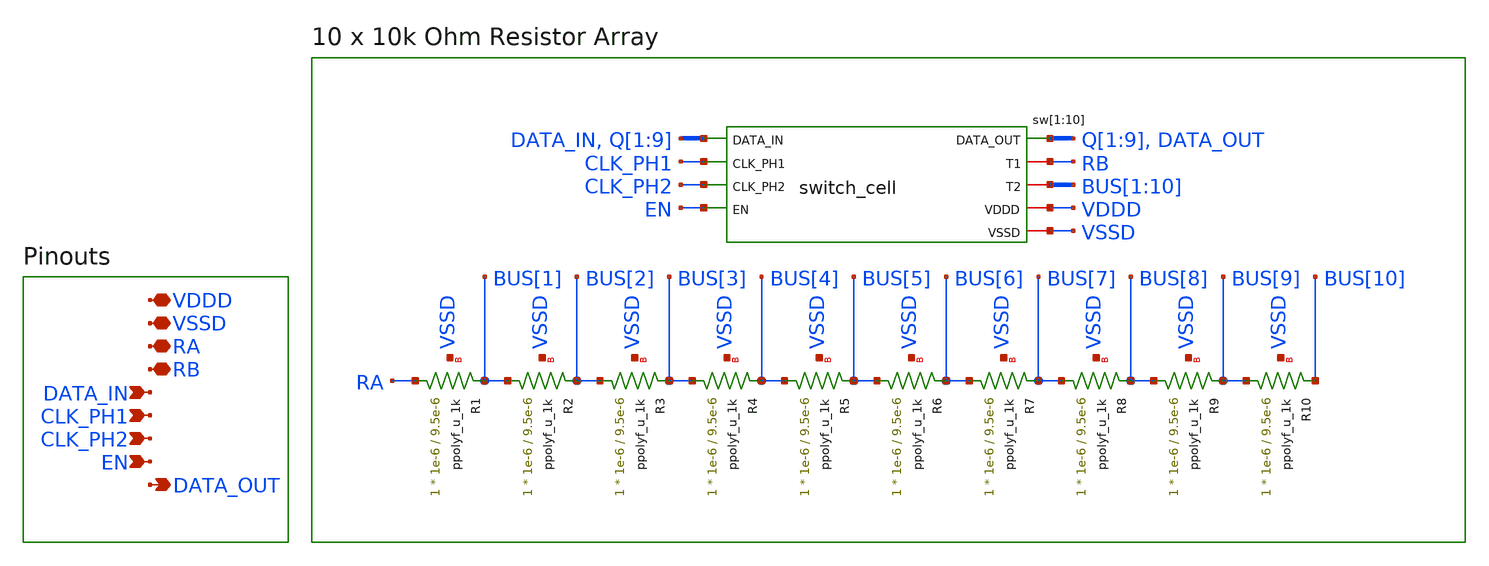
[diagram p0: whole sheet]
** sch_path: designs/libs/core_passive_array/array_res_10x10k/array_res_10x10k.sch
**.subckt array_res_10x10k RA RB VDDD VSSD DATA_IN CLK_PH1 CLK_PH2 EN DATA_OUT
*.iopin RA
*.iopin RB
*.iopin VDDD
*.iopin VSSD
*.ipin DATA_IN
*.ipin CLK_PH1
*.ipin CLK_PH2
*.ipin EN
*.opin DATA_OUT
XR1 RA BUS[1] VSSD ppolyf_u_1k r_width=1e-6 r_length=9.5e-6 m=1
XR2 BUS[1] BUS[2] VSSD ppolyf_u_1k r_width=1e-6 r_length=9.5e-6 m=1
XR3 BUS[2] BUS[3] VSSD ppolyf_u_1k r_width=1e-6 r_length=9.5e-6 m=1
XR4 BUS[3] BUS[4] VSSD ppolyf_u_1k r_width=1e-6 r_length=9.5e-6 m=1
XR5 BUS[4] BUS[5] VSSD ppolyf_u_1k r_width=1e-6 r_length=9.5e-6 m=1
XR6 BUS[5] BUS[6] VSSD ppolyf_u_1k r_width=1e-6 r_length=9.5e-6 m=1
XR7 BUS[6] BUS[7] VSSD ppolyf_u_1k r_width=1e-6 r_length=9.5e-6 m=1
XR8 BUS[7] BUS[8] VSSD ppolyf_u_1k r_width=1e-6 r_length=9.5e-6 m=1
XR9 BUS[8] BUS[9] VSSD ppolyf_u_1k r_width=1e-6 r_length=9.5e-6 m=1
XR10 BUS[9] BUS[10] VSSD ppolyf_u_1k r_width=1e-6 r_length=9.5e-6 m=1
sw[1] DATA_IN CLK_PH1 CLK_PH2 EN Q[1] RB BUS[1] VDDD VSSD switch_cell
sw[2] Q[1] CLK_PH1 CLK_PH2 EN Q[2] RB BUS[2] VDDD VSSD switch_cell
sw[3] Q[2] CLK_PH1 CLK_PH2 EN Q[3] RB BUS[3] VDDD VSSD switch_cell
sw[4] Q[3] CLK_PH1 CLK_PH2 EN Q[4] RB BUS[4] VDDD VSSD switch_cell
sw[5] Q[4] CLK_PH1 CLK_PH2 EN Q[5] RB BUS[5] VDDD VSSD switch_cell
sw[6] Q[5] CLK_PH1 CLK_PH2 EN Q[6] RB BUS[6] VDDD VSSD switch_cell
sw[7] Q[6] CLK_PH1 CLK_PH2 EN Q[7] RB BUS[7] VDDD VSSD switch_cell
sw[8] Q[7] CLK_PH1 CLK_PH2 EN Q[8] RB BUS[8] VDDD VSSD switch_cell
sw[9] Q[8] CLK_PH1 CLK_PH2 EN Q[9] RB BUS[9] VDDD VSSD switch_cell
sw[10] Q[9] CLK_PH1 CLK_PH2 EN DATA_OUT RB BUS[10] VDDD VSSD switch_cell
**.ends

* expanding   symbol:  libs/core_switch_matrix/switch_cell/switch_cell.sym # of pins=9
** sym_path: designs/libs/core_switch_matrix/switch_cell/switch_cell.sym
** sch_path: designs/libs/core_switch_matrix/switch_cell/switch_cell.sch
.subckt switch_cell DATA_IN CLK_PH1 CLK_PH2 EN DATA_OUT T1 T2 VDDD VSSD
*.ipin DATA_IN
*.ipin CLK_PH1
*.ipin CLK_PH2
*.opin DATA_OUT
*.iopin VDDD
*.iopin VSSD
*.ipin EN
*.iopin T1
*.iopin T2
x1 DATA_IN CLK_PH1 CLK_PH2 DATA_OUT VDDD VSSD dff_2ph_clk
x2 DATA_OUT EN VDDD VSSD T1 T2 tgate
.ends


* expanding   symbol:  libs/core_switch_matrix/dff_2ph_clk/dff_2ph_clk.sym # of pins=6
** sym_path: designs/libs/core_switch_matrix/dff_2ph_clk/dff_2ph_clk.sym
** sch_path: designs/libs/core_switch_matrix/dff_2ph_clk/dff_2ph_clk.sch
.subckt dff_2ph_clk D CLK_PH1 CLK_PH2 Q VDDD VSSD
*.ipin D
*.ipin CLK_PH1
*.ipin CLK_PH2
*.opin Q
*.iopin VDDD
*.iopin VSSD
x1 D CLK_PH1 net1 VDDD VDDD VSSD VSSD gf180mcu_fd_sc_mcu9t5v0__latq_1
x2 net1 CLK_PH2 Q VDDD VDDD VSSD VSSD gf180mcu_fd_sc_mcu9t5v0__latq_1
**** begin user architecture code

.include /foss/pdks/gf180mcuD/libs.ref/gf180mcu_fd_sc_mcu9t5v0/spice/gf180mcu_fd_sc_mcu9t5v0.spice

**** end user architecture code
.ends


* expanding   symbol:  libs/core_switch_matrix/tgate/tgate.sym # of pins=6
** sym_path: designs/libs/core_switch_matrix/tgate/tgate.sym
** sch_path: designs/libs/core_switch_matrix/tgate/tgate.sch
.subckt tgate CON EN VDDD VSSD T1 T2
*.ipin CON
*.ipin EN
*.iopin VDDD
*.iopin VSSD
*.iopin T1
*.iopin T2
XM1 T2 NCON T1 VSSD nfet_03v3 L=0.28u W=4u nf=1 ad='int((nf+1)/2) * W/nf * 0.18u' as='int((nf+2)/2) * W/nf * 0.18u'
+ pd='2*int((nf+1)/2) * (W/nf + 0.18u)' ps='2*int((nf+2)/2) * (W/nf + 0.18u)' nrd='0.18u / W' nrs='0.18u / W'
+ sa=0 sb=0 sd=0 m=6
XM2 T2 PCON T1 VDDD pfet_03v3 L=0.28u W=4u nf=1 ad='int((nf+1)/2) * W/nf * 0.18u' as='int((nf+2)/2) * W/nf * 0.18u'
+ pd='2*int((nf+1)/2) * (W/nf + 0.18u)' ps='2*int((nf+2)/2) * (W/nf + 0.18u)' nrd='0.18u / W' nrs='0.18u / W'
+ sa=0 sb=0 sd=0 m=18
x1 CON EN VSSD VDDD VSSD VDDD net1 gf180mcu_fd_sc_mcu9t5v0__nand2_1
x2 net1 VSSD VDDD VSSD VDDD NCON gf180mcu_fd_sc_mcu9t5v0__inv_1
x3 NCON VSSD VDDD VSSD VDDD PCON gf180mcu_fd_sc_mcu9t5v0__inv_1
**** begin user architecture code

.include /foss/pdks/gf180mcuD/libs.ref/gf180mcu_fd_sc_mcu9t5v0/spice/gf180mcu_fd_sc_mcu9t5v0.spice

**** end user architecture code
.ends

.end
